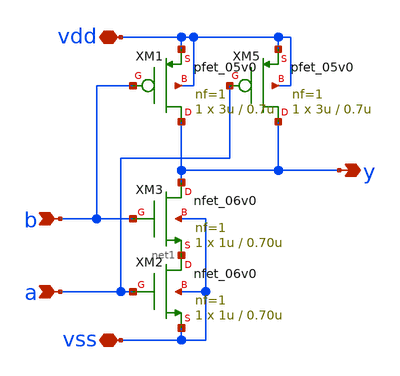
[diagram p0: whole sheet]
** sch_path: member_project/ice458/dynamic_comparator/xschem/nand_5v.sch
**.subckt nand_5v vdd vss a b y
*.iopin vdd
*.iopin vss
*.ipin a
*.ipin b
*.opin y
XM3 y b net1 vss nfet_06v0 L=0.70u W=1u nf=1 ad='int((nf+1)/2) * W/nf * 0.18u' as='int((nf+2)/2) * W/nf * 0.18u'
+ pd='2*int((nf+1)/2) * (W/nf + 0.18u)' ps='2*int((nf+2)/2) * (W/nf + 0.18u)' nrd='0.18u / W' nrs='0.18u / W'
+ sa=0 sb=0 sd=0 m=1
XM5 y a vdd vdd pfet_05v0 L=0.7u W=3u nf=1 ad='int((nf+1)/2) * W/nf * 0.18u' as='int((nf+2)/2) * W/nf * 0.18u'
+ pd='2*int((nf+1)/2) * (W/nf + 0.18u)' ps='2*int((nf+2)/2) * (W/nf + 0.18u)' nrd='0.18u / W' nrs='0.18u / W'
+ sa=0 sb=0 sd=0 m=1
XM1 y b vdd vdd pfet_05v0 L=0.7u W=3u nf=1 ad='int((nf+1)/2) * W/nf * 0.18u' as='int((nf+2)/2) * W/nf * 0.18u'
+ pd='2*int((nf+1)/2) * (W/nf + 0.18u)' ps='2*int((nf+2)/2) * (W/nf + 0.18u)' nrd='0.18u / W' nrs='0.18u / W'
+ sa=0 sb=0 sd=0 m=1
XM2 net1 a vss vss nfet_06v0 L=0.70u W=1u nf=1 ad='int((nf+1)/2) * W/nf * 0.18u' as='int((nf+2)/2) * W/nf * 0.18u'
+ pd='2*int((nf+1)/2) * (W/nf + 0.18u)' ps='2*int((nf+2)/2) * (W/nf + 0.18u)' nrd='0.18u / W' nrs='0.18u / W'
+ sa=0 sb=0 sd=0 m=1
**.ends
.end
